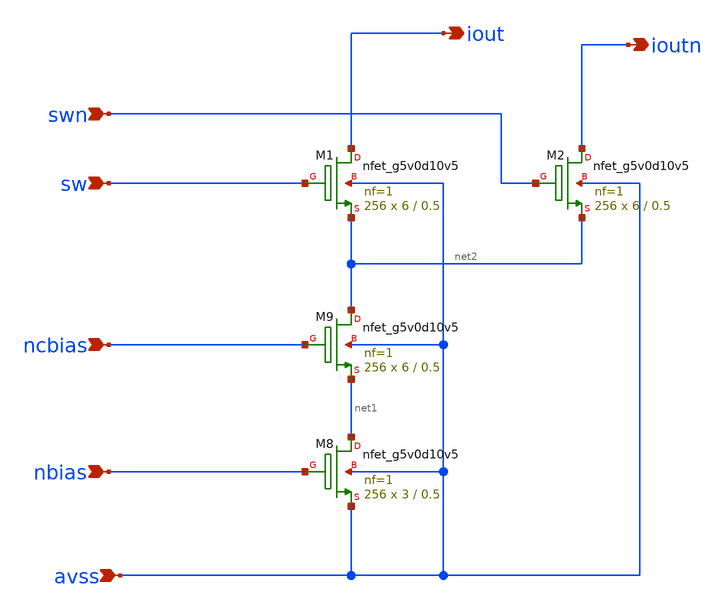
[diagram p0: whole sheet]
** sch_path: xschem/ncell256scs.sch
**.subckt ncell256scs sw ncbias nbias avss iout ioutn swn
*.ipin sw
*.ipin ncbias
*.ipin nbias
*.ipin avss
*.opin iout
*.opin ioutn
*.ipin swn
XM8 net1 nbias avss avss sky130_fd_pr__nfet_g5v0d10v5 L=0.5 W=3 nf=1 ad='int((nf+1)/2) * W/nf * 0.29'
+ as='int((nf+2)/2) * W/nf * 0.29' pd='2*int((nf+1)/2) * (W/nf + 0.29)' ps='2*int((nf+2)/2) * (W/nf + 0.29)'
+ nrd='0.29 / W' nrs='0.29 / W' sa=0 sb=0 sd=0 mult=256 m=256
XM9 net2 ncbias net1 avss sky130_fd_pr__nfet_g5v0d10v5 L=0.5 W=6 nf=1 ad='int((nf+1)/2) * W/nf * 0.29'
+ as='int((nf+2)/2) * W/nf * 0.29' pd='2*int((nf+1)/2) * (W/nf + 0.29)' ps='2*int((nf+2)/2) * (W/nf + 0.29)'
+ nrd='0.29 / W' nrs='0.29 / W' sa=0 sb=0 sd=0 mult=256 m=256
XM1 iout sw net2 avss sky130_fd_pr__nfet_g5v0d10v5 L=0.5 W=6 nf=1 ad='int((nf+1)/2) * W/nf * 0.29' as='int((nf+2)/2) * W/nf * 0.29'
+ pd='2*int((nf+1)/2) * (W/nf + 0.29)' ps='2*int((nf+2)/2) * (W/nf + 0.29)' nrd='0.29 / W' nrs='0.29 / W'
+ sa=0 sb=0 sd=0 mult=256 m=256
XM2 ioutn swn net2 avss sky130_fd_pr__nfet_g5v0d10v5 L=0.5 W=6 nf=1 ad='int((nf+1)/2) * W/nf * 0.29'
+ as='int((nf+2)/2) * W/nf * 0.29' pd='2*int((nf+1)/2) * (W/nf + 0.29)' ps='2*int((nf+2)/2) * (W/nf + 0.29)'
+ nrd='0.29 / W' nrs='0.29 / W' sa=0 sb=0 sd=0 mult=256 m=256
**.ends
.end
